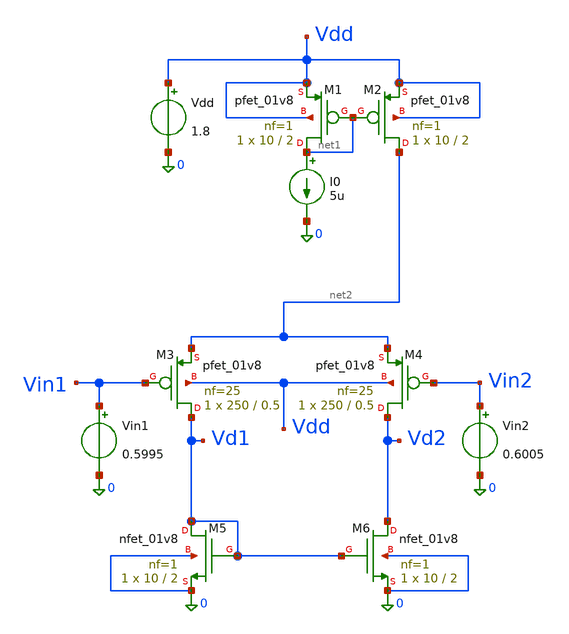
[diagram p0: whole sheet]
** sch_path: stage1/schematics/mirror_diffpair_activeload.sch
**.subckt mirror_diffpair_activeload
I0 net1 0 5u
XM1 net1 net1 Vdd Vdd sky130_fd_pr__pfet_01v8 L=2 W=10 nf=1 ad='int((1 + 1)/2) * 10 / 1 * 0.29' as='int((1 + 2)/2) * 10 / 1 * 0.29'
+ pd='2*int((1 + 1)/2) * (10 / 1 + 0.29)' ps='2*int((1 + 2)/2) * (10 / 1 + 0.29)' nrd='0.29 / 10 ' nrs='0.29 / 10 '
+ sa=0 sb=0 sd=0 mult=1 m=1
XM2 net2 net1 Vdd Vdd sky130_fd_pr__pfet_01v8 L=2 W=10 nf=1 ad='int((1 + 1)/2) * 10 / 1 * 0.29' as='int((1 + 2)/2) * 10 / 1 * 0.29'
+ pd='2*int((1 + 1)/2) * (10 / 1 + 0.29)' ps='2*int((1 + 2)/2) * (10 / 1 + 0.29)' nrd='0.29 / 10 ' nrs='0.29 / 10 '
+ sa=0 sb=0 sd=0 mult=1 m=1
Vdd Vdd 0 1.8
XM3 Vd1 Vin1 net2 Vdd sky130_fd_pr__pfet_01v8 L=0.5 W=250 nf=25 ad='int((25 + 1)/2) * 250 / 25 * 0.29'
+ as='int((25 + 2)/2) * 250 / 25 * 0.29' pd='2*int((25 + 1)/2) * (250 / 25 + 0.29)' ps='2*int((25 + 2)/2) * (250 / 25 + 0.29)'
+ nrd='0.29 / 250 ' nrs='0.29 / 250 ' sa=0 sb=0 sd=0 mult=1 m=1
XM4 Vd2 Vin2 net2 Vdd sky130_fd_pr__pfet_01v8 L=0.5 W=250 nf=25 ad='int((25 + 1)/2) * 250 / 25 * 0.29'
+ as='int((25 + 2)/2) * 250 / 25 * 0.29' pd='2*int((25 + 1)/2) * (250 / 25 + 0.29)' ps='2*int((25 + 2)/2) * (250 / 25 + 0.29)'
+ nrd='0.29 / 250 ' nrs='0.29 / 250 ' sa=0 sb=0 sd=0 mult=1 m=1
Vin1 Vin1 0 0.5995
XM5 Vd1 Vd1 0 0 sky130_fd_pr__nfet_01v8 L=2 W=10 nf=1 ad='int((1 + 1)/2) * 10 / 1 * 0.29' as='int((1 + 2)/2) * 10 / 1 * 0.29'
+ pd='2*int((1 + 1)/2) * (10 / 1 + 0.29)' ps='2*int((1 + 2)/2) * (10 / 1 + 0.29)' nrd='0.29 / 10 ' nrs='0.29 / 10 '
+ sa=0 sb=0 sd=0 mult=1 m=1
XM6 Vd2 Vd1 0 0 sky130_fd_pr__nfet_01v8 L=2 W=10 nf=1 ad='int((1 + 1)/2) * 10 / 1 * 0.29' as='int((1 + 2)/2) * 10 / 1 * 0.29'
+ pd='2*int((1 + 1)/2) * (10 / 1 + 0.29)' ps='2*int((1 + 2)/2) * (10 / 1 + 0.29)' nrd='0.29 / 10 ' nrs='0.29 / 10 '
+ sa=0 sb=0 sd=0 mult=1 m=1
Vin2 Vin2 0 0.6005
**** begin user architecture code

** opencircuitdesign pdks install
.lib $::SKYWATER_MODELS/sky130.lib.spice tt


.include mirror_diffpair_activeload.save
.options savecurrents

.control
	save all
	op
	write initial.raw
	print 1/(@m.xm6.msky130_fd_pr__nfet_01v8[gds])
.endc

**** end user architecture code
**.ends
.end
